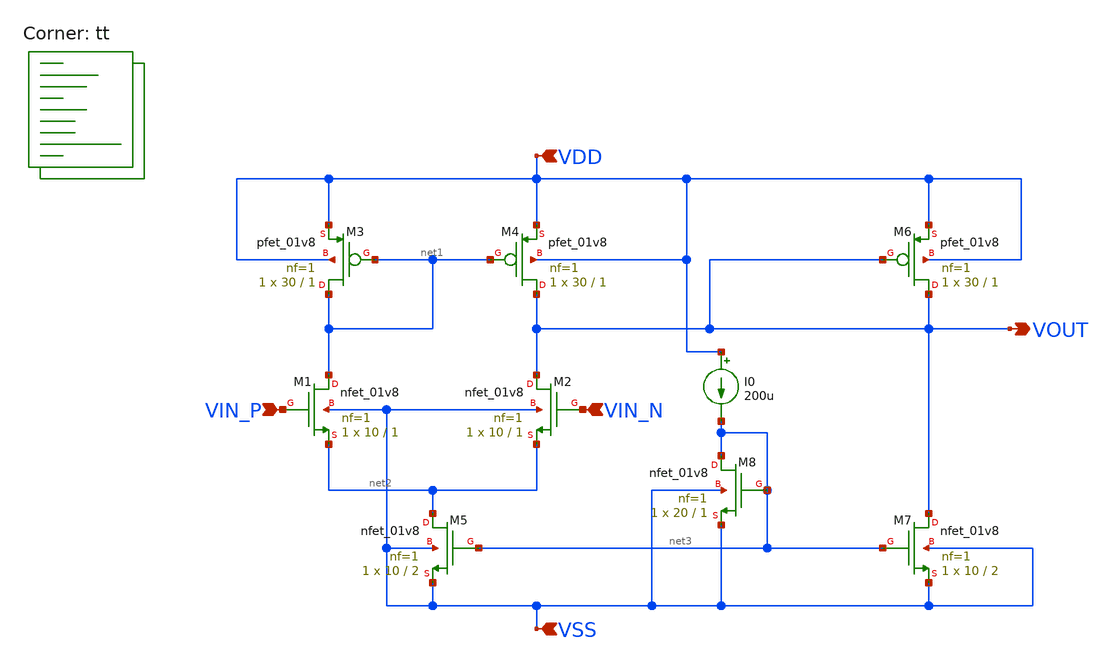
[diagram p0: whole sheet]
** sch_path: analog/schematics/bootcamp_opamp.sch
**.subckt bootcamp_opamp VIN_P VIN_N VDD VSS VOUT
*.ipin VIN_P
*.ipin VIN_N
*.ipin VDD
*.ipin VSS
*.opin VOUT
XM1 net1 VIN_P net2 VSS sky130_fd_pr__nfet_01v8 L=1 W=10 nf=1 ad='int((nf+1)/2) * W/nf * 0.29' as='int((nf+2)/2) * W/nf * 0.29'
+ pd='2*int((nf+1)/2) * (W/nf + 0.29)' ps='2*int((nf+2)/2) * (W/nf + 0.29)' nrd='0.29 / W' nrs='0.29 / W'
+ sa=0 sb=0 sd=0 mult=1 m=1
XM2 VOUT VIN_N net2 VSS sky130_fd_pr__nfet_01v8 L=1 W=10 nf=1 ad='int((nf+1)/2) * W/nf * 0.29' as='int((nf+2)/2) * W/nf * 0.29'
+ pd='2*int((nf+1)/2) * (W/nf + 0.29)' ps='2*int((nf+2)/2) * (W/nf + 0.29)' nrd='0.29 / W' nrs='0.29 / W'
+ sa=0 sb=0 sd=0 mult=1 m=1
XM3 net1 net1 VDD VDD sky130_fd_pr__pfet_01v8 L=1 W=30 nf=1 ad='int((nf+1)/2) * W/nf * 0.29' as='int((nf+2)/2) * W/nf * 0.29'
+ pd='2*int((nf+1)/2) * (W/nf + 0.29)' ps='2*int((nf+2)/2) * (W/nf + 0.29)' nrd='0.29 / W' nrs='0.29 / W'
+ sa=0 sb=0 sd=0 mult=1 m=1
XM4 VOUT net1 VDD VDD sky130_fd_pr__pfet_01v8 L=1 W=30 nf=1 ad='int((nf+1)/2) * W/nf * 0.29' as='int((nf+2)/2) * W/nf * 0.29'
+ pd='2*int((nf+1)/2) * (W/nf + 0.29)' ps='2*int((nf+2)/2) * (W/nf + 0.29)' nrd='0.29 / W' nrs='0.29 / W'
+ sa=0 sb=0 sd=0 mult=1 m=1
XM5 net2 net3 VSS VSS sky130_fd_pr__nfet_01v8 L=2 W=10 nf=1 ad='int((nf+1)/2) * W/nf * 0.29' as='int((nf+2)/2) * W/nf * 0.29'
+ pd='2*int((nf+1)/2) * (W/nf + 0.29)' ps='2*int((nf+2)/2) * (W/nf + 0.29)' nrd='0.29 / W' nrs='0.29 / W'
+ sa=0 sb=0 sd=0 mult=1 m=1
XM6 VOUT VOUT VDD VDD sky130_fd_pr__pfet_01v8 L=1 W=30 nf=1 ad='int((nf+1)/2) * W/nf * 0.29' as='int((nf+2)/2) * W/nf * 0.29'
+ pd='2*int((nf+1)/2) * (W/nf + 0.29)' ps='2*int((nf+2)/2) * (W/nf + 0.29)' nrd='0.29 / W' nrs='0.29 / W'
+ sa=0 sb=0 sd=0 mult=1 m=1
XM7 VOUT net3 VSS VSS sky130_fd_pr__nfet_01v8 L=2 W=10 nf=1 ad='int((nf+1)/2) * W/nf * 0.29' as='int((nf+2)/2) * W/nf * 0.29'
+ pd='2*int((nf+1)/2) * (W/nf + 0.29)' ps='2*int((nf+2)/2) * (W/nf + 0.29)' nrd='0.29 / W' nrs='0.29 / W'
+ sa=0 sb=0 sd=0 mult=1 m=1
XM8 net3 net3 VSS VSS sky130_fd_pr__nfet_01v8 L=1 W=20 nf=1 ad='int((nf+1)/2) * W/nf * 0.29' as='int((nf+2)/2) * W/nf * 0.29'
+ pd='2*int((nf+1)/2) * (W/nf + 0.29)' ps='2*int((nf+2)/2) * (W/nf + 0.29)' nrd='0.29 / W' nrs='0.29 / W'
+ sa=0 sb=0 sd=0 mult=1 m=1
I0 VDD net3 200u
**** begin user architecture code
.lib $::SKYWATER_MODELS/sky130.lib.spice tt
**** end user architecture code
**.ends
.end
